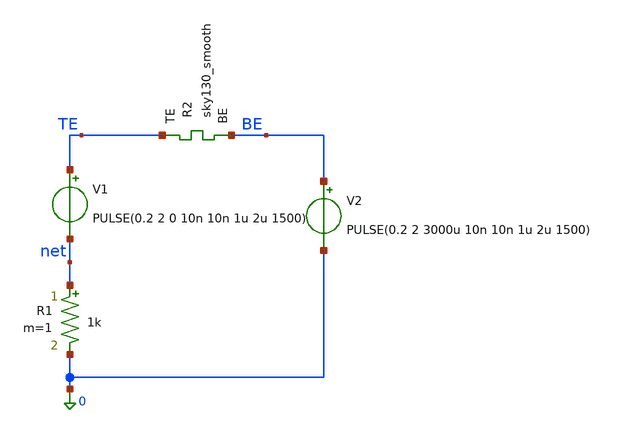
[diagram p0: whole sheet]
** sch_path: memristor_models/sky130_smooth/tb_1R_smooth.sch
**.subckt tb_1R_smooth
V1 TE net PULSE(0.2 2 0 10n 10n 1u 2u 1500)
R1 net 0 1k m=1
XR2 TE BE sky130_smooth Tfilament_0=3.3e-9
V2 BE 0 PULSE(0.2 2 3000u 10n 10n 1u 2u 1500)
**** begin user architecture code

** opencircuitdesign pdks install
.inc $::SKYWATER_MODELS/sky130_smooth.spice



.option savecurrents
.tran 100n 6000u
.control
	save all
	run
	write tb_1R_smooth.raw
.endc



**** end user architecture code
**.ends
.end
